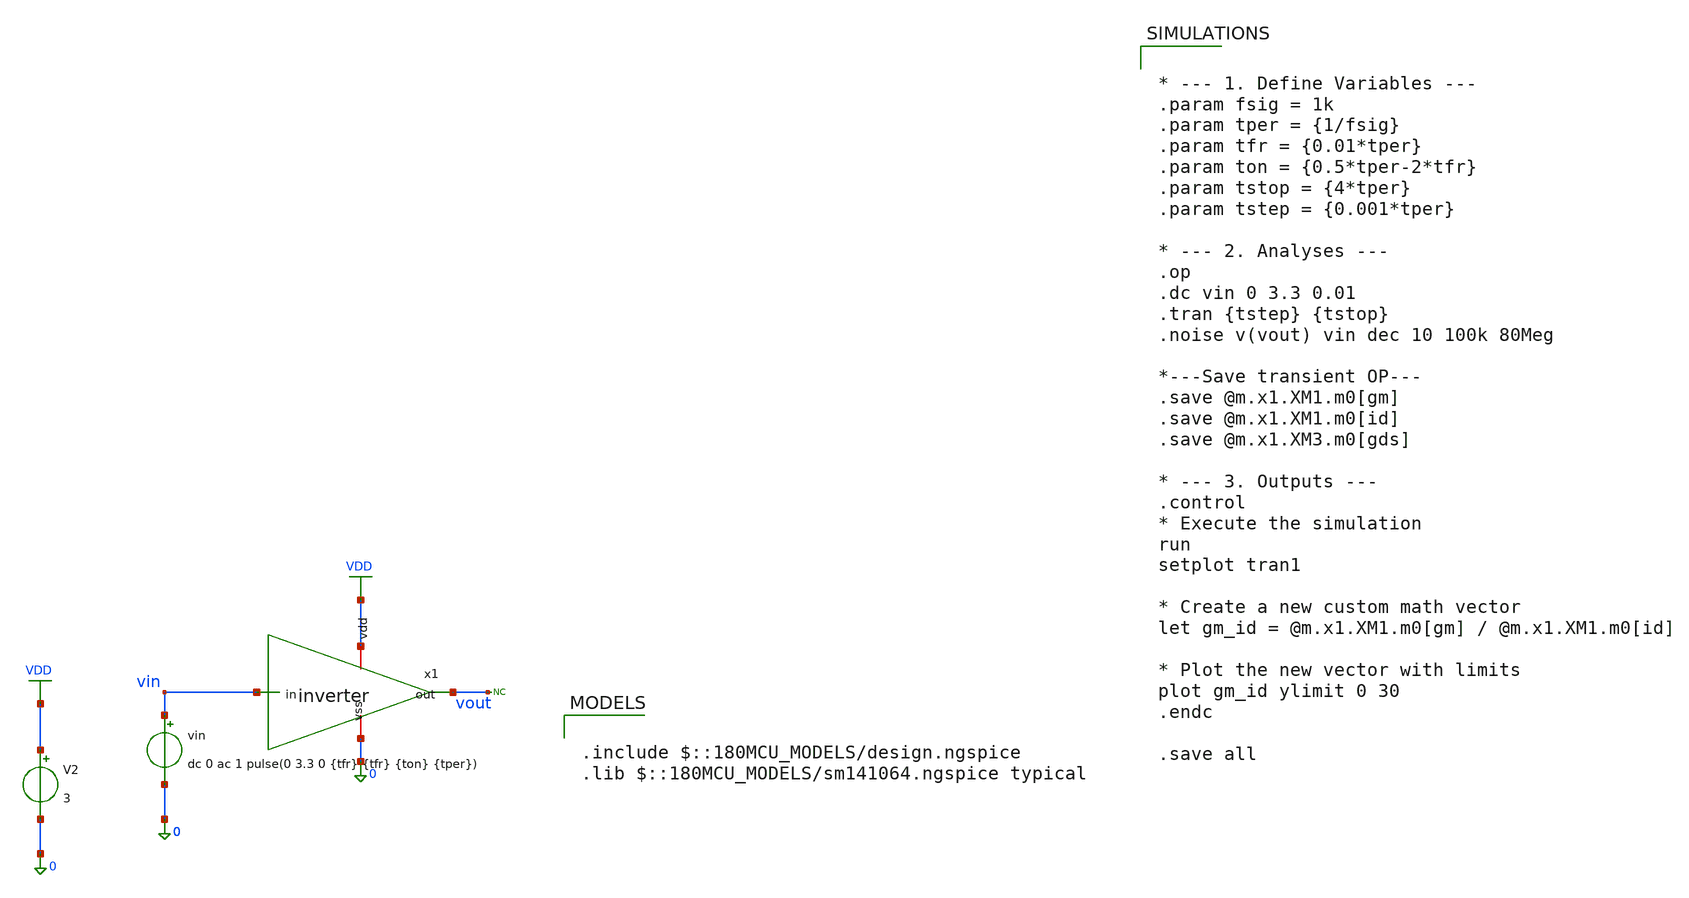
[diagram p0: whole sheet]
** sch_path: Marcel/designs/TB_Inverter.sch
**.subckt TB_Inverter
x1 vin vout 0 VDD inverter
vin vin 0 dc 0 ac 1 pulse(0 3.3 0 {tfr} {tfr} {ton} {tper})
V2 VDD 0 3
* noconn vout
**** begin user architecture code

.include $::180MCU_MODELS/design.ngspice
.lib $::180MCU_MODELS/sm141064.ngspice typical



* --- 1. Define Variables ---
.param fsig = 1k
.param tper = {1/fsig}
.param tfr = {0.01*tper}
.param ton = {0.5*tper-2*tfr}
.param tstop = {4*tper}
.param tstep = {0.001*tper}

* --- 2. Analyses ---
.op
.dc vin 0 3.3 0.01
.tran {tstep} {tstop}
.noise v(vout) vin dec 10 100k 80Meg

*---Save transient OP---
.save @m.x1.XM1.m0[gm]
.save @m.x1.XM1.m0[id]
.save @m.x1.XM3.m0[gds]

* --- 3. Outputs ---
.control
* Execute the simulation
run
setplot tran1

* Create a new custom math vector
let gm_id = @m.x1.XM1.m0[gm] / @m.x1.XM1.m0[id]

* Plot the new vector with limits
plot gm_id ylimit 0 30
.endc

.save all


**** end user architecture code
**.ends
.GLOBAL VDD
.end
